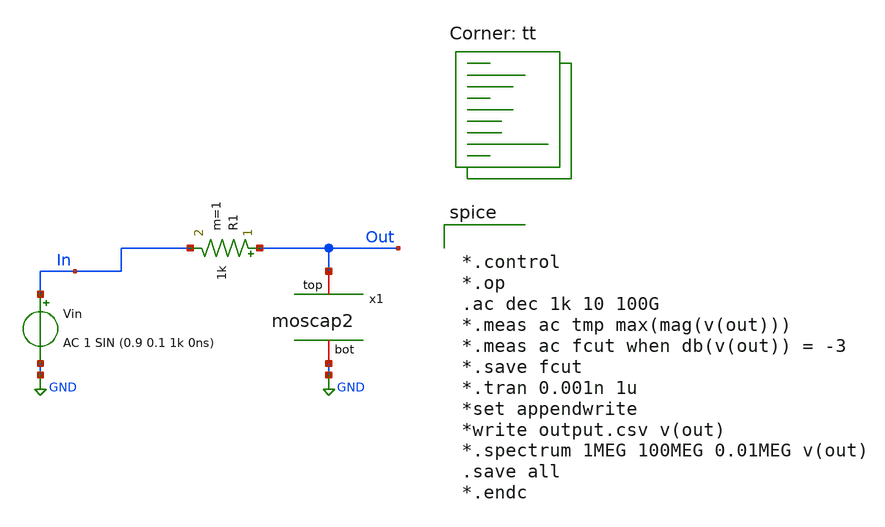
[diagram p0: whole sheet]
** sch_path: CAP/moscap2_tb.sch
**.subckt moscap2_tb
R1 Out In 1k m=1
Vin In GND AC 1 SIN (0.9 0.1 1k 0ns)
x1 GND Out moscap2
**** begin user architecture code
.lib $::SKYWATER_MODELS/sky130.lib.spice tt


*.control
*.op
.ac dec 1k 10 100G
*.meas ac tmp max(mag(v(out)))
*.meas ac fcut when db(v(out)) = -3
*.save fcut
*.tran 0.001n 1u
*set appendwrite
*write output.csv v(out)
*.spectrum 1MEG 100MEG 0.01MEG v(out)
.save all
*.endc


**** end user architecture code
**.ends

* expanding   symbol:  project/CAP/moscap2.sym # of pins=2
** sym_path: CAP/moscap2.sym
** sch_path: CAP/moscap2.sch
.subckt moscap2 bot top
*.iopin bot
*.iopin top
XM1 bot top bot bot sky130_fd_pr__nfet_01v8 L=0.5 W=2 nf=1 ad='int((nf+1)/2) * W/nf * 0.29' as='int((nf+2)/2) * W/nf * 0.29'
+ pd='2*int((nf+1)/2) * (W/nf + 0.29)' ps='2*int((nf+2)/2) * (W/nf + 0.29)' nrd='0.29 / W' nrs='0.29 / W'
+ sa=0 sb=0 sd=0 mult=4 m=4
.ends

.GLOBAL GND
.end
